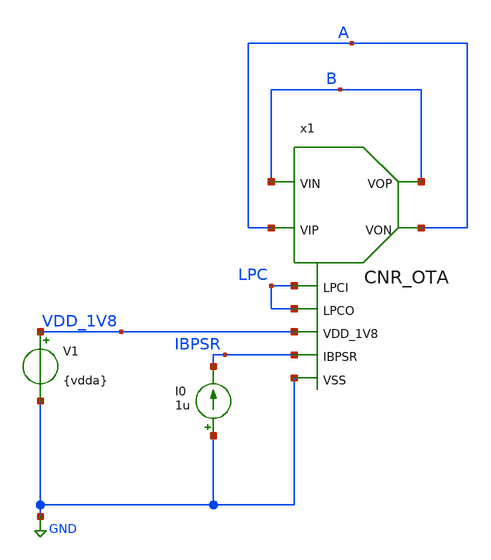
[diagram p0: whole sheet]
** sch_path: work/TB_CNR_OTA.sch
**.subckt TB_CNR_OTA
x1 VDD_1V8 B A B A IBPSR GND LPC LPC CNR_OTA
V1 VDD_1V8 GND {vdda}
I0 GND IBPSR 1u
**** begin user architecture code



* ngspice commands
.include corner.spi



**** end user architecture code
**.ends
.GLOBAL GND
.end
